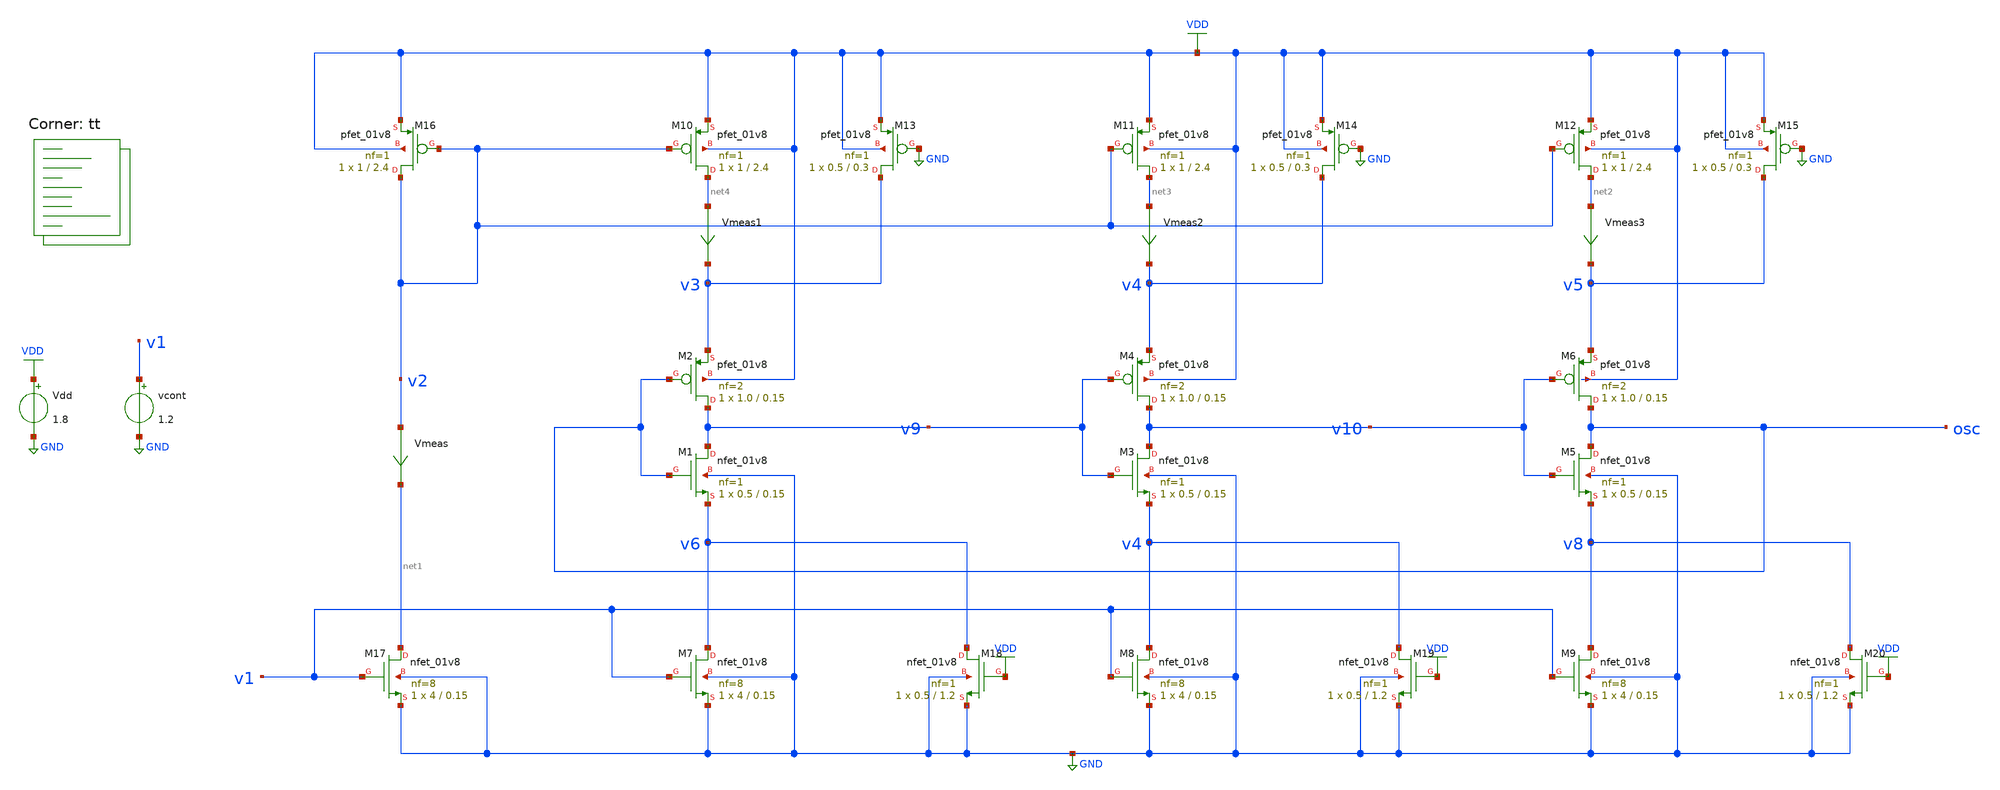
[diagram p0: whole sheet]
** sch_path: projects/pll/vco/xschem_ngspice/tb_current_starved_VCO6.sch
**.subckt tb_current_starved_VCO6
XM1 v9 osc v6 GND sky130_fd_pr__nfet_01v8 L=0.15 W=0.5 nf=1 ad='int((nf+1)/2) * W/nf * 0.29' as='int((nf+2)/2) * W/nf * 0.29'
+ pd='2*int((nf+1)/2) * (W/nf + 0.29)' ps='2*int((nf+2)/2) * (W/nf + 0.29)' nrd='0.29 / W' nrs='0.29 / W'
+ sa=0 sb=0 sd=0 mult=1 m=1
XM2 v9 osc v3 VDD sky130_fd_pr__pfet_01v8 L=0.15 W=1.0 nf=2 ad='int((nf+1)/2) * W/nf * 0.29' as='int((nf+2)/2) * W/nf * 0.29'
+ pd='2*int((nf+1)/2) * (W/nf + 0.29)' ps='2*int((nf+2)/2) * (W/nf + 0.29)' nrd='0.29 / W' nrs='0.29 / W'
+ sa=0 sb=0 sd=0 mult=1 m=1
XM3 v10 v9 v4 GND sky130_fd_pr__nfet_01v8 L=0.15 W=0.5 nf=1 ad='int((nf+1)/2) * W/nf * 0.29' as='int((nf+2)/2) * W/nf * 0.29'
+ pd='2*int((nf+1)/2) * (W/nf + 0.29)' ps='2*int((nf+2)/2) * (W/nf + 0.29)' nrd='0.29 / W' nrs='0.29 / W'
+ sa=0 sb=0 sd=0 mult=1 m=1
XM4 v10 v9 v4 VDD sky130_fd_pr__pfet_01v8 L=0.15 W=1.0 nf=2 ad='int((nf+1)/2) * W/nf * 0.29' as='int((nf+2)/2) * W/nf * 0.29'
+ pd='2*int((nf+1)/2) * (W/nf + 0.29)' ps='2*int((nf+2)/2) * (W/nf + 0.29)' nrd='0.29 / W' nrs='0.29 / W'
+ sa=0 sb=0 sd=0 mult=1 m=1
XM5 osc v10 v8 GND sky130_fd_pr__nfet_01v8 L=0.15 W=0.5 nf=1 ad='int((nf+1)/2) * W/nf * 0.29' as='int((nf+2)/2) * W/nf * 0.29'
+ pd='2*int((nf+1)/2) * (W/nf + 0.29)' ps='2*int((nf+2)/2) * (W/nf + 0.29)' nrd='0.29 / W' nrs='0.29 / W'
+ sa=0 sb=0 sd=0 mult=1 m=1
XM6 osc v10 v5 VDD sky130_fd_pr__pfet_01v8 L=0.15 W=1.0 nf=2 ad='int((nf+1)/2) * W/nf * 0.29' as='int((nf+2)/2) * W/nf * 0.29'
+ pd='2*int((nf+1)/2) * (W/nf + 0.29)' ps='2*int((nf+2)/2) * (W/nf + 0.29)' nrd='0.29 / W' nrs='0.29 / W'
+ sa=0 sb=0 sd=0 mult=1 m=1
XM7 v6 v1 GND GND sky130_fd_pr__nfet_01v8 L=0.15 W=4 nf=8 ad='int((nf+1)/2) * W/nf * 0.29' as='int((nf+2)/2) * W/nf * 0.29'
+ pd='2*int((nf+1)/2) * (W/nf + 0.29)' ps='2*int((nf+2)/2) * (W/nf + 0.29)' nrd='0.29 / W' nrs='0.29 / W'
+ sa=0 sb=0 sd=0 mult=1 m=1
XM8 v4 v1 GND GND sky130_fd_pr__nfet_01v8 L=0.15 W=4 nf=8 ad='int((nf+1)/2) * W/nf * 0.29' as='int((nf+2)/2) * W/nf * 0.29'
+ pd='2*int((nf+1)/2) * (W/nf + 0.29)' ps='2*int((nf+2)/2) * (W/nf + 0.29)' nrd='0.29 / W' nrs='0.29 / W'
+ sa=0 sb=0 sd=0 mult=1 m=1
XM9 v8 v1 GND GND sky130_fd_pr__nfet_01v8 L=0.15 W=4 nf=8 ad='int((nf+1)/2) * W/nf * 0.29' as='int((nf+2)/2) * W/nf * 0.29'
+ pd='2*int((nf+1)/2) * (W/nf + 0.29)' ps='2*int((nf+2)/2) * (W/nf + 0.29)' nrd='0.29 / W' nrs='0.29 / W'
+ sa=0 sb=0 sd=0 mult=1 m=1
Vdd VDD GND 1.8
vcont v1 GND 1.2
XM18 v6 VDD GND GND sky130_fd_pr__nfet_01v8 L=1.2 W=0.5 nf=1 ad='int((nf+1)/2) * W/nf * 0.29' as='int((nf+2)/2) * W/nf * 0.29'
+ pd='2*int((nf+1)/2) * (W/nf + 0.29)' ps='2*int((nf+2)/2) * (W/nf + 0.29)' nrd='0.29 / W' nrs='0.29 / W'
+ sa=0 sb=0 sd=0 mult=1 m=1
XM19 v4 VDD GND GND sky130_fd_pr__nfet_01v8 L=1.2 W=0.5 nf=1 ad='int((nf+1)/2) * W/nf * 0.29' as='int((nf+2)/2) * W/nf * 0.29'
+ pd='2*int((nf+1)/2) * (W/nf + 0.29)' ps='2*int((nf+2)/2) * (W/nf + 0.29)' nrd='0.29 / W' nrs='0.29 / W'
+ sa=0 sb=0 sd=0 mult=1 m=1
XM20 v8 VDD GND GND sky130_fd_pr__nfet_01v8 L=1.2 W=0.5 nf=1 ad='int((nf+1)/2) * W/nf * 0.29' as='int((nf+2)/2) * W/nf * 0.29'
+ pd='2*int((nf+1)/2) * (W/nf + 0.29)' ps='2*int((nf+2)/2) * (W/nf + 0.29)' nrd='0.29 / W' nrs='0.29 / W'
+ sa=0 sb=0 sd=0 mult=1 m=1
XM10 net4 v2 VDD VDD sky130_fd_pr__pfet_01v8 L=2.4 W=1 nf=1 ad='int((nf+1)/2) * W/nf * 0.29' as='int((nf+2)/2) * W/nf * 0.29'
+ pd='2*int((nf+1)/2) * (W/nf + 0.29)' ps='2*int((nf+2)/2) * (W/nf + 0.29)' nrd='0.29 / W' nrs='0.29 / W'
+ sa=0 sb=0 sd=0 mult=1 m=1
XM11 net3 v2 VDD VDD sky130_fd_pr__pfet_01v8 L=2.4 W=1 nf=1 ad='int((nf+1)/2) * W/nf * 0.29' as='int((nf+2)/2) * W/nf * 0.29'
+ pd='2*int((nf+1)/2) * (W/nf + 0.29)' ps='2*int((nf+2)/2) * (W/nf + 0.29)' nrd='0.29 / W' nrs='0.29 / W'
+ sa=0 sb=0 sd=0 mult=1 m=1
XM12 net2 v2 VDD VDD sky130_fd_pr__pfet_01v8 L=2.4 W=1 nf=1 ad='int((nf+1)/2) * W/nf * 0.29' as='int((nf+2)/2) * W/nf * 0.29'
+ pd='2*int((nf+1)/2) * (W/nf + 0.29)' ps='2*int((nf+2)/2) * (W/nf + 0.29)' nrd='0.29 / W' nrs='0.29 / W'
+ sa=0 sb=0 sd=0 mult=1 m=1
XM13 v3 GND VDD VDD sky130_fd_pr__pfet_01v8 L=0.3 W=0.5 nf=1 ad='int((nf+1)/2) * W/nf * 0.29' as='int((nf+2)/2) * W/nf * 0.29'
+ pd='2*int((nf+1)/2) * (W/nf + 0.29)' ps='2*int((nf+2)/2) * (W/nf + 0.29)' nrd='0.29 / W' nrs='0.29 / W'
+ sa=0 sb=0 sd=0 mult=1 m=1
XM14 v4 GND VDD VDD sky130_fd_pr__pfet_01v8 L=0.3 W=0.5 nf=1 ad='int((nf+1)/2) * W/nf * 0.29' as='int((nf+2)/2) * W/nf * 0.29'
+ pd='2*int((nf+1)/2) * (W/nf + 0.29)' ps='2*int((nf+2)/2) * (W/nf + 0.29)' nrd='0.29 / W' nrs='0.29 / W'
+ sa=0 sb=0 sd=0 mult=1 m=1
XM15 v5 GND VDD VDD sky130_fd_pr__pfet_01v8 L=0.3 W=0.5 nf=1 ad='int((nf+1)/2) * W/nf * 0.29' as='int((nf+2)/2) * W/nf * 0.29'
+ pd='2*int((nf+1)/2) * (W/nf + 0.29)' ps='2*int((nf+2)/2) * (W/nf + 0.29)' nrd='0.29 / W' nrs='0.29 / W'
+ sa=0 sb=0 sd=0 mult=1 m=1
XM16 v2 v2 VDD VDD sky130_fd_pr__pfet_01v8 L=2.4 W=1 nf=1 ad='int((nf+1)/2) * W/nf * 0.29' as='int((nf+2)/2) * W/nf * 0.29'
+ pd='2*int((nf+1)/2) * (W/nf + 0.29)' ps='2*int((nf+2)/2) * (W/nf + 0.29)' nrd='0.29 / W' nrs='0.29 / W'
+ sa=0 sb=0 sd=0 mult=1 m=1
XM17 net1 v1 GND GND sky130_fd_pr__nfet_01v8 L=0.15 W=4 nf=8 ad='int((nf+1)/2) * W/nf * 0.29' as='int((nf+2)/2) * W/nf * 0.29'
+ pd='2*int((nf+1)/2) * (W/nf + 0.29)' ps='2*int((nf+2)/2) * (W/nf + 0.29)' nrd='0.29 / W' nrs='0.29 / W'
+ sa=0 sb=0 sd=0 mult=1 m=1
Vmeas v2 net1 0
.save i(vmeas)
Vmeas1 net4 v3 0
.save i(vmeas1)
Vmeas2 net3 v4 0
.save i(vmeas2)
Vmeas3 net2 v5 0
.save i(vmeas3)
**** begin user architecture code
.lib $::SKYWATER_MODELS/sky130.lib.spice tt



.option method=gear
.option wnflag=1


*.ic v(vcont)=1.2

*.temp = 75

* Xmeasure osc freq2 measure_Kvco thresh=0.9 dir=1

.control

  * pre_osdi ./measure_Kvco.osdi

  let v_cont_start = 0.0
  let v_cont_stop = 1.9

  dowhile v_cont_start <= v_cont_stop
    alter vcont $&v_cont_start
    *save v(vcont) v(osc) v(vout) v(v1) v(v2) i(vmeas) i(vmeas1)
    save all
    tran 1ps 30ns
    remzerovec
    write tb_current_starved_VCO6_{$&v_cont_start}.raw
    * write tb_current_starved_VCO6.raw
    linearize v(osc)
    let filename = v_cont_start * 100
    wrdata /foss/designs/my_design/projects/pll/vco/xschem_ngspice/tb_current_starved_VCO6_{$&filename}.txt
+ v(osc)
    set appendwrite

    reset
    let v_cont_start = v_cont_start + 0.1
  end
.endc




**** end user architecture code
**.ends
.GLOBAL GND
.GLOBAL VDD
.end
